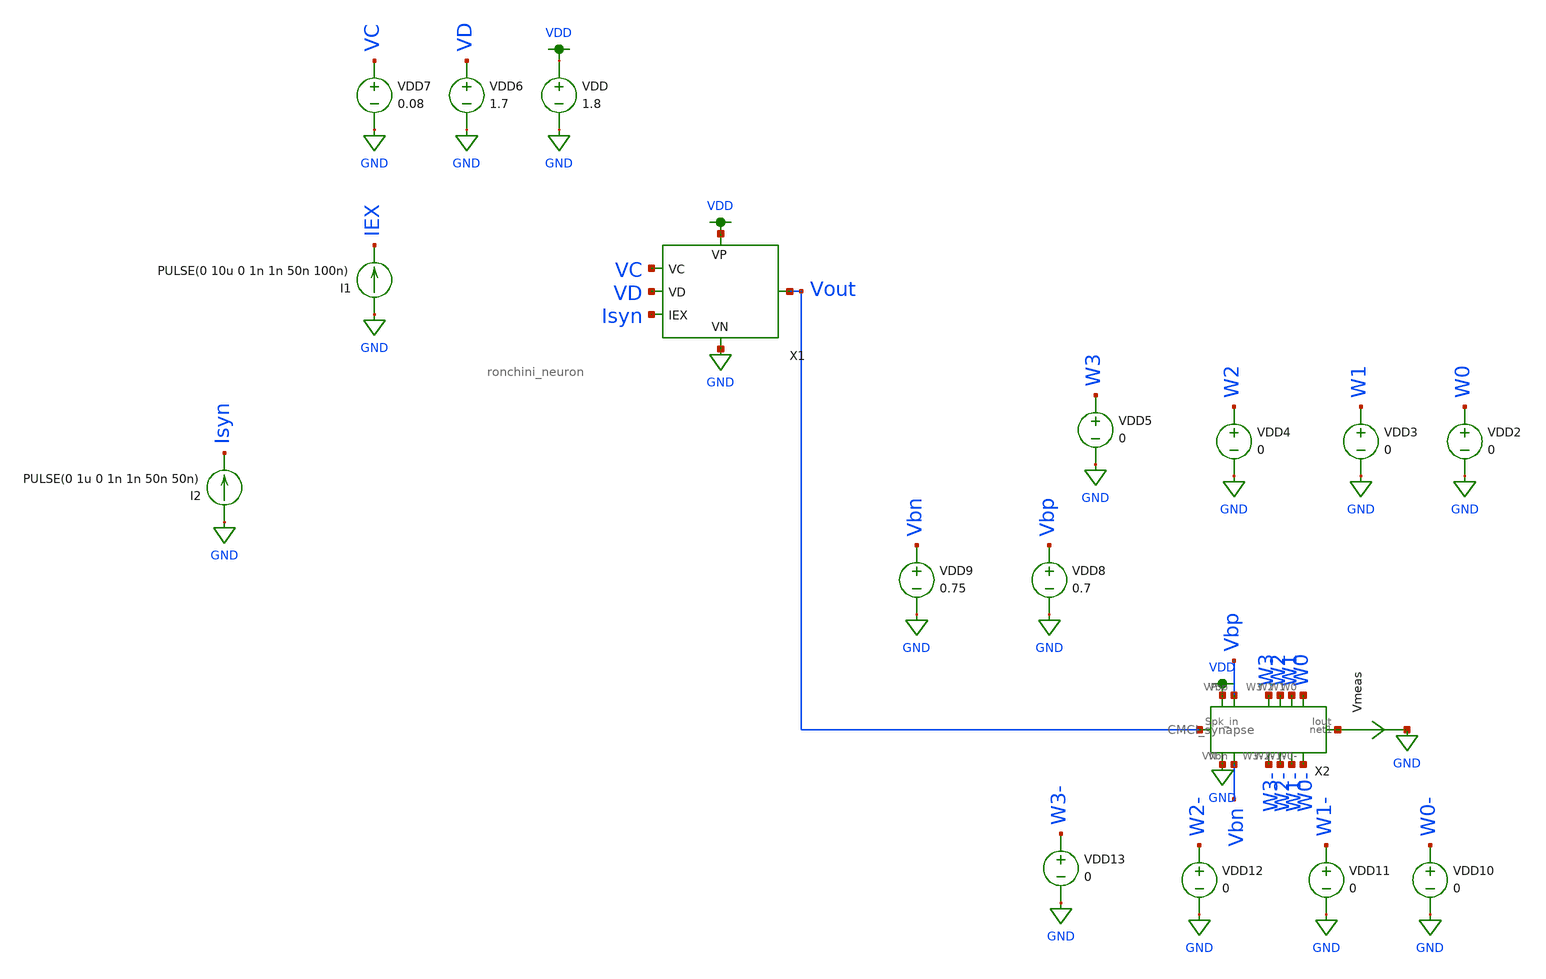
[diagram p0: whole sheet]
** sch_path: schematic/ronchini_neuron_tran.sch
**.subckt ronchini_neuron_tran
VDD VDD GND 1.8
I1 GND IEX PULSE(0 10u 0 1n 1n 50n 100n)
VDD6 VD GND 1.7
VDD7 VC GND 0.08
X1 VC VD Isyn GND VDD Vout ronchini_neuron
VDD2 W0 GND 0
VDD3 W1 GND 0
VDD4 W2 GND 0
VDD5 W3 GND 0
VDD8 Vbp GND 0.7
VDD9 Vbn GND 0.75
VDD10 W0- GND 0
VDD11 W1- GND 0
VDD12 W2- GND 0
VDD13 W3- GND 0
Vmeas net1 GND 0
.save i(vmeas)
X2 VDD Vbp W3 W2 W1 W0 net1 W0- W1- W2- W3- Vbn GND Vout CMCI_synapse
I2 GND Isyn PULSE(0 1u 0 1n 1n 50n 50n)
**** begin user architecture code

.param W=12
.param L=0.5
.tran 0.1n 10u
.save all


.option wnflag=1
.param MC_SWITCH=0.0
.lib ~/skywater/skywater-pdk/libraries/sky130_fd_pr_ngspice/latest/models/sky130.lib.spice tt

**** end user architecture code
**.ends
.GLOBAL GND
.GLOBAL VDD
.end
